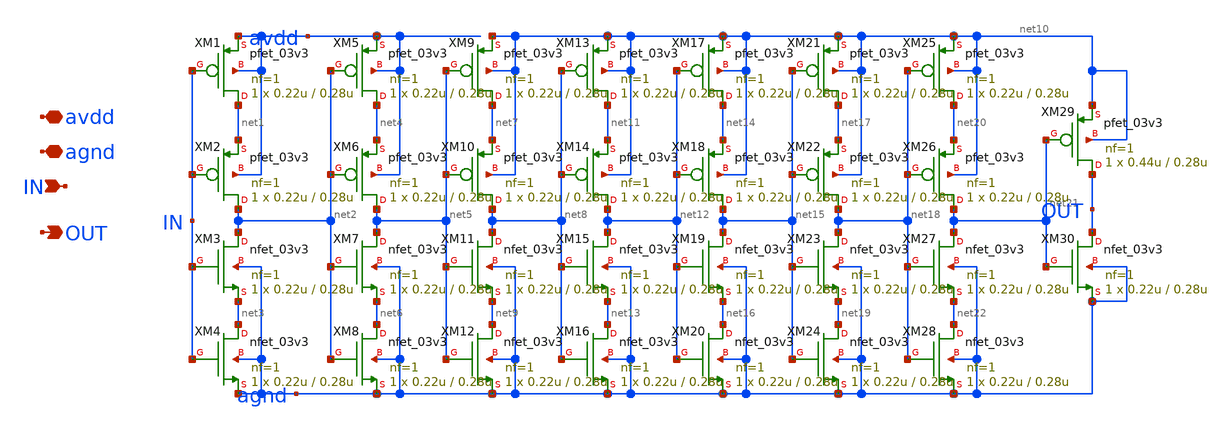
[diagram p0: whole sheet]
** sch_path: mpw18h1/cisar-gen/xschem/TBD/Delay.sch
**.subckt Delay agnd IN OUT avdd
*.iopin agnd
*.ipin IN
*.opin OUT
*.iopin avdd
XM1 net1 IN avdd avdd pfet_03v3 L=0.28u W=0.22u nf=1 ad='int((nf+1)/2) * W/nf * 0.18u' as='int((nf+2)/2) * W/nf * 0.18u'
+ pd='2*int((nf+1)/2) * (W/nf + 0.18u)' ps='2*int((nf+2)/2) * (W/nf + 0.18u)' nrd='0.18u / W' nrs='0.18u / W'
+ sa=0 sb=0 sd=0 m=1
XM2 net2 IN net1 avdd pfet_03v3 L=0.28u W=0.22u nf=1 ad='int((nf+1)/2) * W/nf * 0.18u' as='int((nf+2)/2) * W/nf * 0.18u'
+ pd='2*int((nf+1)/2) * (W/nf + 0.18u)' ps='2*int((nf+2)/2) * (W/nf + 0.18u)' nrd='0.18u / W' nrs='0.18u / W'
+ sa=0 sb=0 sd=0 m=1
XM3 net2 IN net3 agnd nfet_03v3 L=0.28u W=0.22u nf=1 ad='int((nf+1)/2) * W/nf * 0.18u' as='int((nf+2)/2) * W/nf * 0.18u'
+ pd='2*int((nf+1)/2) * (W/nf + 0.18u)' ps='2*int((nf+2)/2) * (W/nf + 0.18u)' nrd='0.18u / W' nrs='0.18u / W'
+ sa=0 sb=0 sd=0 m=1
XM4 net3 IN agnd agnd nfet_03v3 L=0.28u W=0.22u nf=1 ad='int((nf+1)/2) * W/nf * 0.18u' as='int((nf+2)/2) * W/nf * 0.18u'
+ pd='2*int((nf+1)/2) * (W/nf + 0.18u)' ps='2*int((nf+2)/2) * (W/nf + 0.18u)' nrd='0.18u / W' nrs='0.18u / W'
+ sa=0 sb=0 sd=0 m=1
XM5 net4 net2 avdd avdd pfet_03v3 L=0.28u W=0.22u nf=1 ad='int((nf+1)/2) * W/nf * 0.18u' as='int((nf+2)/2) * W/nf * 0.18u'
+ pd='2*int((nf+1)/2) * (W/nf + 0.18u)' ps='2*int((nf+2)/2) * (W/nf + 0.18u)' nrd='0.18u / W' nrs='0.18u / W'
+ sa=0 sb=0 sd=0 m=1
XM6 net5 net2 net4 avdd pfet_03v3 L=0.28u W=0.22u nf=1 ad='int((nf+1)/2) * W/nf * 0.18u' as='int((nf+2)/2) * W/nf * 0.18u'
+ pd='2*int((nf+1)/2) * (W/nf + 0.18u)' ps='2*int((nf+2)/2) * (W/nf + 0.18u)' nrd='0.18u / W' nrs='0.18u / W'
+ sa=0 sb=0 sd=0 m=1
XM7 net5 net2 net6 agnd nfet_03v3 L=0.28u W=0.22u nf=1 ad='int((nf+1)/2) * W/nf * 0.18u' as='int((nf+2)/2) * W/nf * 0.18u'
+ pd='2*int((nf+1)/2) * (W/nf + 0.18u)' ps='2*int((nf+2)/2) * (W/nf + 0.18u)' nrd='0.18u / W' nrs='0.18u / W'
+ sa=0 sb=0 sd=0 m=1
XM8 net6 net2 agnd agnd nfet_03v3 L=0.28u W=0.22u nf=1 ad='int((nf+1)/2) * W/nf * 0.18u' as='int((nf+2)/2) * W/nf * 0.18u'
+ pd='2*int((nf+1)/2) * (W/nf + 0.18u)' ps='2*int((nf+2)/2) * (W/nf + 0.18u)' nrd='0.18u / W' nrs='0.18u / W'
+ sa=0 sb=0 sd=0 m=1
XM9 net7 net5 net10 net10 pfet_03v3 L=0.28u W=0.22u nf=1 ad='int((nf+1)/2) * W/nf * 0.18u' as='int((nf+2)/2) * W/nf * 0.18u'
+ pd='2*int((nf+1)/2) * (W/nf + 0.18u)' ps='2*int((nf+2)/2) * (W/nf + 0.18u)' nrd='0.18u / W' nrs='0.18u / W'
+ sa=0 sb=0 sd=0 m=1
XM10 net8 net5 net7 net10 pfet_03v3 L=0.28u W=0.22u nf=1 ad='int((nf+1)/2) * W/nf * 0.18u' as='int((nf+2)/2) * W/nf * 0.18u'
+ pd='2*int((nf+1)/2) * (W/nf + 0.18u)' ps='2*int((nf+2)/2) * (W/nf + 0.18u)' nrd='0.18u / W' nrs='0.18u / W'
+ sa=0 sb=0 sd=0 m=1
XM11 net8 net5 net9 agnd nfet_03v3 L=0.28u W=0.22u nf=1 ad='int((nf+1)/2) * W/nf * 0.18u' as='int((nf+2)/2) * W/nf * 0.18u'
+ pd='2*int((nf+1)/2) * (W/nf + 0.18u)' ps='2*int((nf+2)/2) * (W/nf + 0.18u)' nrd='0.18u / W' nrs='0.18u / W'
+ sa=0 sb=0 sd=0 m=1
XM12 net9 net5 agnd agnd nfet_03v3 L=0.28u W=0.22u nf=1 ad='int((nf+1)/2) * W/nf * 0.18u' as='int((nf+2)/2) * W/nf * 0.18u'
+ pd='2*int((nf+1)/2) * (W/nf + 0.18u)' ps='2*int((nf+2)/2) * (W/nf + 0.18u)' nrd='0.18u / W' nrs='0.18u / W'
+ sa=0 sb=0 sd=0 m=1
XM13 net11 net8 net10 net10 pfet_03v3 L=0.28u W=0.22u nf=1 ad='int((nf+1)/2) * W/nf * 0.18u' as='int((nf+2)/2) * W/nf * 0.18u'
+ pd='2*int((nf+1)/2) * (W/nf + 0.18u)' ps='2*int((nf+2)/2) * (W/nf + 0.18u)' nrd='0.18u / W' nrs='0.18u / W'
+ sa=0 sb=0 sd=0 m=1
XM14 net12 net8 net11 net10 pfet_03v3 L=0.28u W=0.22u nf=1 ad='int((nf+1)/2) * W/nf * 0.18u' as='int((nf+2)/2) * W/nf * 0.18u'
+ pd='2*int((nf+1)/2) * (W/nf + 0.18u)' ps='2*int((nf+2)/2) * (W/nf + 0.18u)' nrd='0.18u / W' nrs='0.18u / W'
+ sa=0 sb=0 sd=0 m=1
XM15 net12 net8 net13 agnd nfet_03v3 L=0.28u W=0.22u nf=1 ad='int((nf+1)/2) * W/nf * 0.18u' as='int((nf+2)/2) * W/nf * 0.18u'
+ pd='2*int((nf+1)/2) * (W/nf + 0.18u)' ps='2*int((nf+2)/2) * (W/nf + 0.18u)' nrd='0.18u / W' nrs='0.18u / W'
+ sa=0 sb=0 sd=0 m=1
XM16 net13 net8 agnd agnd nfet_03v3 L=0.28u W=0.22u nf=1 ad='int((nf+1)/2) * W/nf * 0.18u' as='int((nf+2)/2) * W/nf * 0.18u'
+ pd='2*int((nf+1)/2) * (W/nf + 0.18u)' ps='2*int((nf+2)/2) * (W/nf + 0.18u)' nrd='0.18u / W' nrs='0.18u / W'
+ sa=0 sb=0 sd=0 m=1
XM17 net14 net12 net10 net10 pfet_03v3 L=0.28u W=0.22u nf=1 ad='int((nf+1)/2) * W/nf * 0.18u' as='int((nf+2)/2) * W/nf * 0.18u'
+ pd='2*int((nf+1)/2) * (W/nf + 0.18u)' ps='2*int((nf+2)/2) * (W/nf + 0.18u)' nrd='0.18u / W' nrs='0.18u / W'
+ sa=0 sb=0 sd=0 m=1
XM18 net15 net12 net14 net10 pfet_03v3 L=0.28u W=0.22u nf=1 ad='int((nf+1)/2) * W/nf * 0.18u' as='int((nf+2)/2) * W/nf * 0.18u'
+ pd='2*int((nf+1)/2) * (W/nf + 0.18u)' ps='2*int((nf+2)/2) * (W/nf + 0.18u)' nrd='0.18u / W' nrs='0.18u / W'
+ sa=0 sb=0 sd=0 m=1
XM19 net15 net12 net16 agnd nfet_03v3 L=0.28u W=0.22u nf=1 ad='int((nf+1)/2) * W/nf * 0.18u' as='int((nf+2)/2) * W/nf * 0.18u'
+ pd='2*int((nf+1)/2) * (W/nf + 0.18u)' ps='2*int((nf+2)/2) * (W/nf + 0.18u)' nrd='0.18u / W' nrs='0.18u / W'
+ sa=0 sb=0 sd=0 m=1
XM20 net16 net12 agnd agnd nfet_03v3 L=0.28u W=0.22u nf=1 ad='int((nf+1)/2) * W/nf * 0.18u' as='int((nf+2)/2) * W/nf * 0.18u'
+ pd='2*int((nf+1)/2) * (W/nf + 0.18u)' ps='2*int((nf+2)/2) * (W/nf + 0.18u)' nrd='0.18u / W' nrs='0.18u / W'
+ sa=0 sb=0 sd=0 m=1
XM21 net17 net15 net10 net10 pfet_03v3 L=0.28u W=0.22u nf=1 ad='int((nf+1)/2) * W/nf * 0.18u' as='int((nf+2)/2) * W/nf * 0.18u'
+ pd='2*int((nf+1)/2) * (W/nf + 0.18u)' ps='2*int((nf+2)/2) * (W/nf + 0.18u)' nrd='0.18u / W' nrs='0.18u / W'
+ sa=0 sb=0 sd=0 m=1
XM22 net18 net15 net17 net10 pfet_03v3 L=0.28u W=0.22u nf=1 ad='int((nf+1)/2) * W/nf * 0.18u' as='int((nf+2)/2) * W/nf * 0.18u'
+ pd='2*int((nf+1)/2) * (W/nf + 0.18u)' ps='2*int((nf+2)/2) * (W/nf + 0.18u)' nrd='0.18u / W' nrs='0.18u / W'
+ sa=0 sb=0 sd=0 m=1
XM23 net18 net15 net19 agnd nfet_03v3 L=0.28u W=0.22u nf=1 ad='int((nf+1)/2) * W/nf * 0.18u' as='int((nf+2)/2) * W/nf * 0.18u'
+ pd='2*int((nf+1)/2) * (W/nf + 0.18u)' ps='2*int((nf+2)/2) * (W/nf + 0.18u)' nrd='0.18u / W' nrs='0.18u / W'
+ sa=0 sb=0 sd=0 m=1
XM24 net19 net15 agnd agnd nfet_03v3 L=0.28u W=0.22u nf=1 ad='int((nf+1)/2) * W/nf * 0.18u' as='int((nf+2)/2) * W/nf * 0.18u'
+ pd='2*int((nf+1)/2) * (W/nf + 0.18u)' ps='2*int((nf+2)/2) * (W/nf + 0.18u)' nrd='0.18u / W' nrs='0.18u / W'
+ sa=0 sb=0 sd=0 m=1
XM25 net20 net18 net10 net10 pfet_03v3 L=0.28u W=0.22u nf=1 ad='int((nf+1)/2) * W/nf * 0.18u' as='int((nf+2)/2) * W/nf * 0.18u'
+ pd='2*int((nf+1)/2) * (W/nf + 0.18u)' ps='2*int((nf+2)/2) * (W/nf + 0.18u)' nrd='0.18u / W' nrs='0.18u / W'
+ sa=0 sb=0 sd=0 m=1
XM26 net21 net18 net20 net10 pfet_03v3 L=0.28u W=0.22u nf=1 ad='int((nf+1)/2) * W/nf * 0.18u' as='int((nf+2)/2) * W/nf * 0.18u'
+ pd='2*int((nf+1)/2) * (W/nf + 0.18u)' ps='2*int((nf+2)/2) * (W/nf + 0.18u)' nrd='0.18u / W' nrs='0.18u / W'
+ sa=0 sb=0 sd=0 m=1
XM27 net21 net18 net22 agnd nfet_03v3 L=0.28u W=0.22u nf=1 ad='int((nf+1)/2) * W/nf * 0.18u' as='int((nf+2)/2) * W/nf * 0.18u'
+ pd='2*int((nf+1)/2) * (W/nf + 0.18u)' ps='2*int((nf+2)/2) * (W/nf + 0.18u)' nrd='0.18u / W' nrs='0.18u / W'
+ sa=0 sb=0 sd=0 m=1
XM28 net22 net18 agnd agnd nfet_03v3 L=0.28u W=0.22u nf=1 ad='int((nf+1)/2) * W/nf * 0.18u' as='int((nf+2)/2) * W/nf * 0.18u'
+ pd='2*int((nf+1)/2) * (W/nf + 0.18u)' ps='2*int((nf+2)/2) * (W/nf + 0.18u)' nrd='0.18u / W' nrs='0.18u / W'
+ sa=0 sb=0 sd=0 m=1
XM29 OUT net21 net10 net10 pfet_03v3 L=0.28u W=0.44u nf=1 ad='int((nf+1)/2) * W/nf * 0.18u' as='int((nf+2)/2) * W/nf * 0.18u'
+ pd='2*int((nf+1)/2) * (W/nf + 0.18u)' ps='2*int((nf+2)/2) * (W/nf + 0.18u)' nrd='0.18u / W' nrs='0.18u / W'
+ sa=0 sb=0 sd=0 m=1
XM30 OUT net21 agnd agnd nfet_03v3 L=0.28u W=0.22u nf=1 ad='int((nf+1)/2) * W/nf * 0.18u' as='int((nf+2)/2) * W/nf * 0.18u'
+ pd='2*int((nf+1)/2) * (W/nf + 0.18u)' ps='2*int((nf+2)/2) * (W/nf + 0.18u)' nrd='0.18u / W' nrs='0.18u / W'
+ sa=0 sb=0 sd=0 m=1
**.ends
.end
